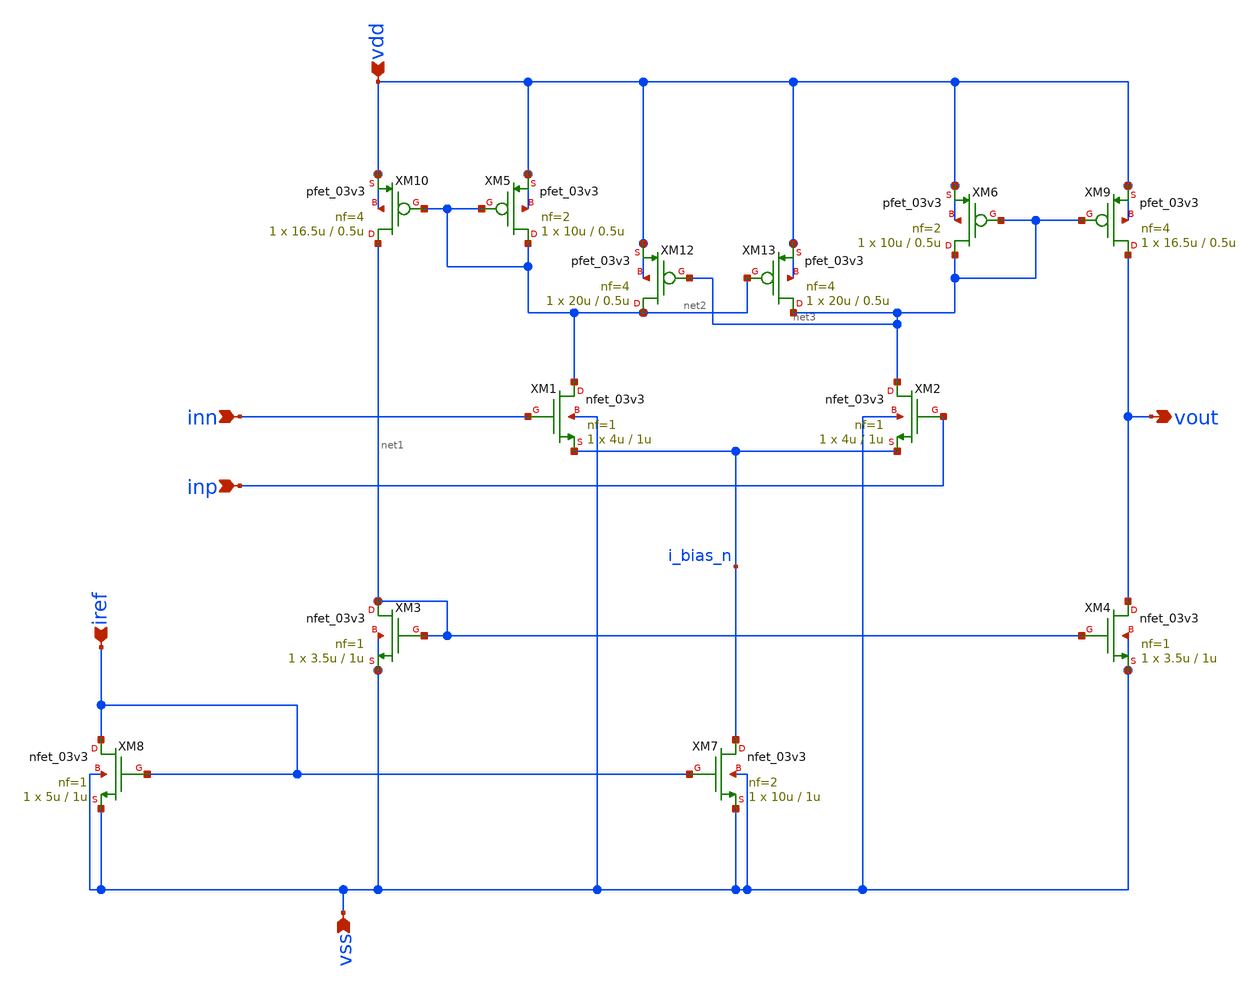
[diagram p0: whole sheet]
** sch_path: designs/libs/core_analog/nmos_comp/nmos_comp.sch
**.subckt nmos_comp vss vdd iref inn inp vout
*.ipin vss
*.ipin vdd
*.ipin iref
*.ipin inn
*.ipin inp
*.opin vout
XM3 net1 net1 vss vss nfet_03v3 L=1u W=3.5u nf=1 ad='int((nf+1)/2) * W/nf * 0.18u' as='int((nf+2)/2) * W/nf * 0.18u'
+ pd='2*int((nf+1)/2) * (W/nf + 0.18u)' ps='2*int((nf+2)/2) * (W/nf + 0.18u)' nrd='0.18u / W' nrs='0.18u / W'
+ sa=0 sb=0 sd=0 m=1
XM4 vout net1 vss vss nfet_03v3 L=1u W=3.5u nf=1 ad='int((nf+1)/2) * W/nf * 0.18u' as='int((nf+2)/2) * W/nf * 0.18u'
+ pd='2*int((nf+1)/2) * (W/nf + 0.18u)' ps='2*int((nf+2)/2) * (W/nf + 0.18u)' nrd='0.18u / W' nrs='0.18u / W'
+ sa=0 sb=0 sd=0 m=1
XM1 net2 inn i_bias_n vss nfet_03v3 L=1u W=4u nf=1 ad='int((nf+1)/2) * W/nf * 0.18u' as='int((nf+2)/2) * W/nf * 0.18u'
+ pd='2*int((nf+1)/2) * (W/nf + 0.18u)' ps='2*int((nf+2)/2) * (W/nf + 0.18u)' nrd='0.18u / W' nrs='0.18u / W'
+ sa=0 sb=0 sd=0 m=1
XM2 net3 inp i_bias_n vss nfet_03v3 L=1u W=4u nf=1 ad='int((nf+1)/2) * W/nf * 0.18u' as='int((nf+2)/2) * W/nf * 0.18u'
+ pd='2*int((nf+1)/2) * (W/nf + 0.18u)' ps='2*int((nf+2)/2) * (W/nf + 0.18u)' nrd='0.18u / W' nrs='0.18u / W'
+ sa=0 sb=0 sd=0 m=1
XM10 net1 net2 vdd vdd pfet_03v3 L=0.5u W=16.5u nf=4 ad='int((nf+1)/2) * W/nf * 0.18u' as='int((nf+2)/2) * W/nf * 0.18u'
+ pd='2*int((nf+1)/2) * (W/nf + 0.18u)' ps='2*int((nf+2)/2) * (W/nf + 0.18u)' nrd='0.18u / W' nrs='0.18u / W'
+ sa=0 sb=0 sd=0 m=1
XM6 net3 net3 vdd vdd pfet_03v3 L=0.5u W=10u nf=2 ad='int((nf+1)/2) * W/nf * 0.18u' as='int((nf+2)/2) * W/nf * 0.18u'
+ pd='2*int((nf+1)/2) * (W/nf + 0.18u)' ps='2*int((nf+2)/2) * (W/nf + 0.18u)' nrd='0.18u / W' nrs='0.18u / W'
+ sa=0 sb=0 sd=0 m=1
XM5 net2 net2 vdd vdd pfet_03v3 L=0.5u W=10u nf=2 ad='int((nf+1)/2) * W/nf * 0.18u' as='int((nf+2)/2) * W/nf * 0.18u'
+ pd='2*int((nf+1)/2) * (W/nf + 0.18u)' ps='2*int((nf+2)/2) * (W/nf + 0.18u)' nrd='0.18u / W' nrs='0.18u / W'
+ sa=0 sb=0 sd=0 m=1
XM9 vout net3 vdd vdd pfet_03v3 L=0.5u W=16.5u nf=4 ad='int((nf+1)/2) * W/nf * 0.18u' as='int((nf+2)/2) * W/nf * 0.18u'
+ pd='2*int((nf+1)/2) * (W/nf + 0.18u)' ps='2*int((nf+2)/2) * (W/nf + 0.18u)' nrd='0.18u / W' nrs='0.18u / W'
+ sa=0 sb=0 sd=0 m=1
XM8 iref iref vss vss nfet_03v3 L=1u W=5u nf=1 ad='int((nf+1)/2) * W/nf * 0.18u' as='int((nf+2)/2) * W/nf * 0.18u'
+ pd='2*int((nf+1)/2) * (W/nf + 0.18u)' ps='2*int((nf+2)/2) * (W/nf + 0.18u)' nrd='0.18u / W' nrs='0.18u / W'
+ sa=0 sb=0 sd=0 m=1
XM7 i_bias_n iref vss vss nfet_03v3 L=1u W=10u nf=2 ad='int((nf+1)/2) * W/nf * 0.18u' as='int((nf+2)/2) * W/nf * 0.18u'
+ pd='2*int((nf+1)/2) * (W/nf + 0.18u)' ps='2*int((nf+2)/2) * (W/nf + 0.18u)' nrd='0.18u / W' nrs='0.18u / W'
+ sa=0 sb=0 sd=0 m=1
XM12 net2 net3 vdd vdd pfet_03v3 L=0.5u W=20u nf=4 ad='int((nf+1)/2) * W/nf * 0.18u' as='int((nf+2)/2) * W/nf * 0.18u'
+ pd='2*int((nf+1)/2) * (W/nf + 0.18u)' ps='2*int((nf+2)/2) * (W/nf + 0.18u)' nrd='0.18u / W' nrs='0.18u / W'
+ sa=0 sb=0 sd=0 m=1
XM13 net3 net2 vdd vdd pfet_03v3 L=0.5u W=20u nf=4 ad='int((nf+1)/2) * W/nf * 0.18u' as='int((nf+2)/2) * W/nf * 0.18u'
+ pd='2*int((nf+1)/2) * (W/nf + 0.18u)' ps='2*int((nf+2)/2) * (W/nf + 0.18u)' nrd='0.18u / W' nrs='0.18u / W'
+ sa=0 sb=0 sd=0 m=1
**.ends
.end
